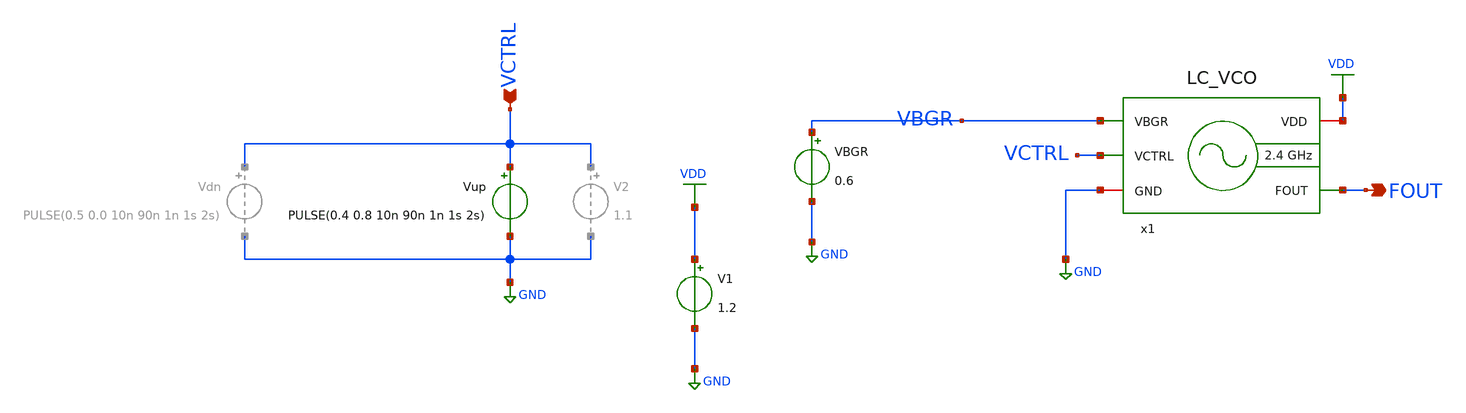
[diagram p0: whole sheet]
** sch_path: xschem/lc-vco/LC_VCO_tb.sch
**.subckt LC_VCO_tb FOUT VCTRL
*.opin FOUT
*.ipin VCTRL
VBGR VBGR GND 0.6
x1 VDD VCTRL GND FOUT VBGR LC_VCO
V1 VDD GND 1.2
Vup VCTRL GND PULSE(0.4 0.8 10n 90n 1n 1s 2s)
**** begin user architecture code



.param temp = 27
.options method=gear rshunt=1.0e12

.control

* Save required signals
save v(VCTRL) v(FOUT) v(x1.Vx) v(x1.OUTp)

* Long transient simulation
tran 10p 500n 100n

* Save raw waveform
write tb_LC_VCO_tran.raw

* Plot transient waveform
let vout = v(FOUT)
plot v(VCTRL) v(x1.Vx) v(FOUT) v(x1.OUTp)

* Plot steady-state waveform
plot v(VCTRL) v(x1.Vx) v(FOUT) v(x1.OUTp) xlimit 400n 405n

* FFT analysis
setplot tran1
linearize vout
set specwindow=blackman
fft vout

* Plot FFT spectrum
let power_out_db = db(vout)
plot power_out_db xlimit 2.34G 2.54G ylimit -200 0

* Find the maximum magnitude value between 2G and 3G
meas sp max_power_out_db max power_out_db FROM=2G TO=3G

* Save FFT spectrum as raw file
write LC_VCO_fft.raw

* Save FFT data
wrdata fft_output_standalone.txt frequency power_out_db

* Save waveform for external processing
wrdata vco_waveform_standalone.txt power_out_db

.endc






.param temp=27
.control
save all
op
write LC_VCO_tb.raw
.endc




.include 4nH_INDUCTOR.spice


.lib cornerMOSlv.lib mos_tt
.lib cornerMOShv.lib mos_tt
.lib cornerRES.lib res_typ
.lib cornerCAP.lib cap_typ

**** end user architecture code
**.ends

* expanding   symbol:  xschem/lc-vco/LC_VCO.sym # of pins=5
** sym_path: xschem/lc-vco/LC_VCO.sym
** sch_path: xschem/lc-vco/LC_VCO.sch
.subckt LC_VCO VDD VCTRL GND FOUT VBGR
*.opin FOUT
*.ipin VCTRL
*.ipin VBGR
*.iopin VDD
*.iopin GND
XM5 Vx Vgs GND GND sg13_lv_nmos w=384u l=1u ng=48 m=1 mm_ok=1
XM4 OUTp OUTn VDD VDD sg13_lv_pmos w=36u l=0.13u ng=5 m=1 mm_ok=1
XM3 OUTn OUTp VDD VDD sg13_lv_pmos w=36u l=0.13u ng=5 m=1 mm_ok=1
XM2 OUTp OUTn Vx GND sg13_lv_nmos w=22u l=0.13u ng=3 m=1 mm_ok=1
XM1 OUTn OUTp Vx GND sg13_lv_nmos w=22u l=0.13u ng=3 m=1 mm_ok=1
XM6 Vgs Vgs GND GND sg13_lv_nmos w=64u l=1u ng=8 m=1 mm_ok=1
XC1 OUTn OUTp GND cap_rfcmim w=21.9e-6 l=21.9e-6 wfeed=10.0e-6 m=1 mm_ok=1
XC3 OUTp VCTRL OUTn GND sg13_hv_svaricap w=9.74u l=0.8u Nx=7
XC2 OUTp VCTRL OUTn GND sg13_hv_svaricap w=9.74u l=0.8u Nx=7
XM7 Vgs VBGR VDD VDD sg13_lv_pmos w=38u l=1u ng=5 m=1 mm_ok=1
XM8 FOUT OUTp VDD VDD sg13_lv_pmos w=15u l=0.13u ng=10 m=1 mm_ok=1
XM9 FOUT OUTp GND GND sg13_lv_nmos w=1.5u l=0.13u ng=1 m=1 mm_ok=1
XM10 net1 OUTn VDD VDD sg13_lv_pmos w=15u l=0.13u ng=10 m=1 mm_ok=1
XM11 net1 OUTn GND GND sg13_lv_nmos w=1.5u l=0.13u ng=1 m=1 mm_ok=1
x2 OUTn OUTp 4nH_INDUCTOR
.ends

.GLOBAL GND
.GLOBAL VDD
.end
